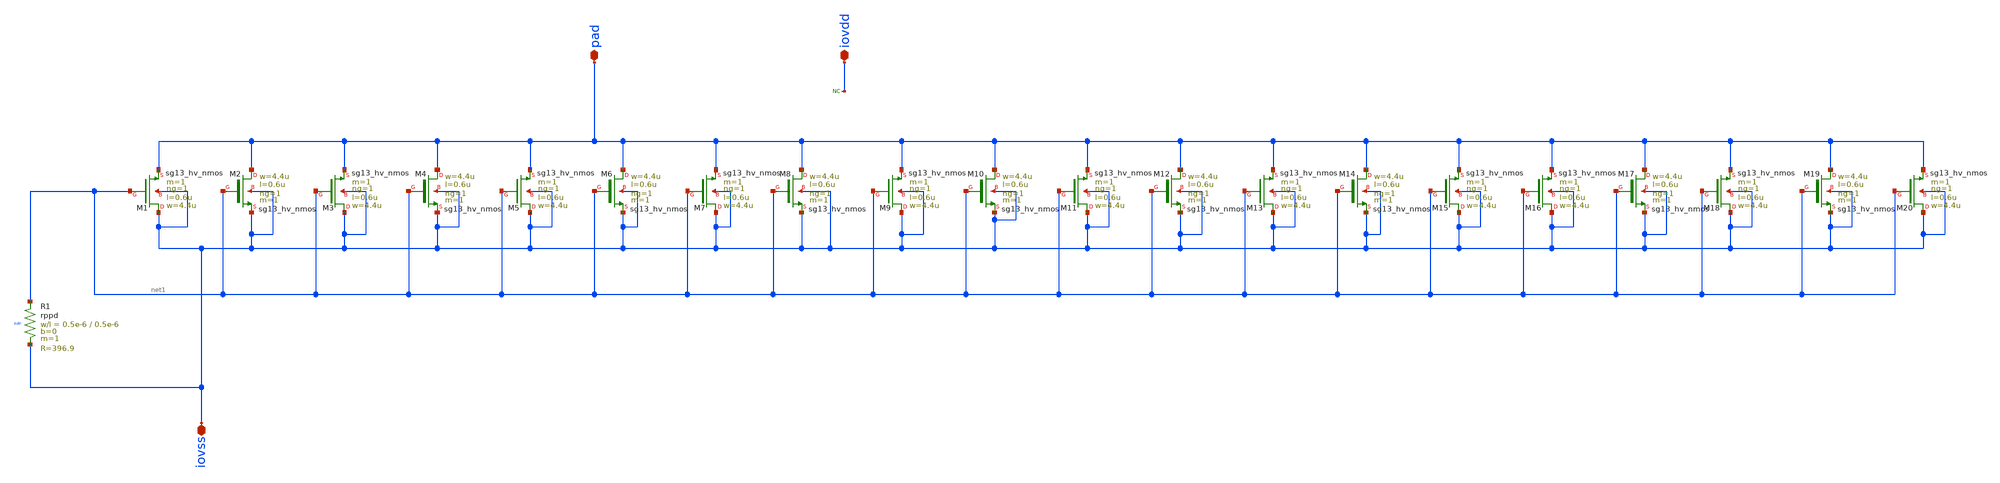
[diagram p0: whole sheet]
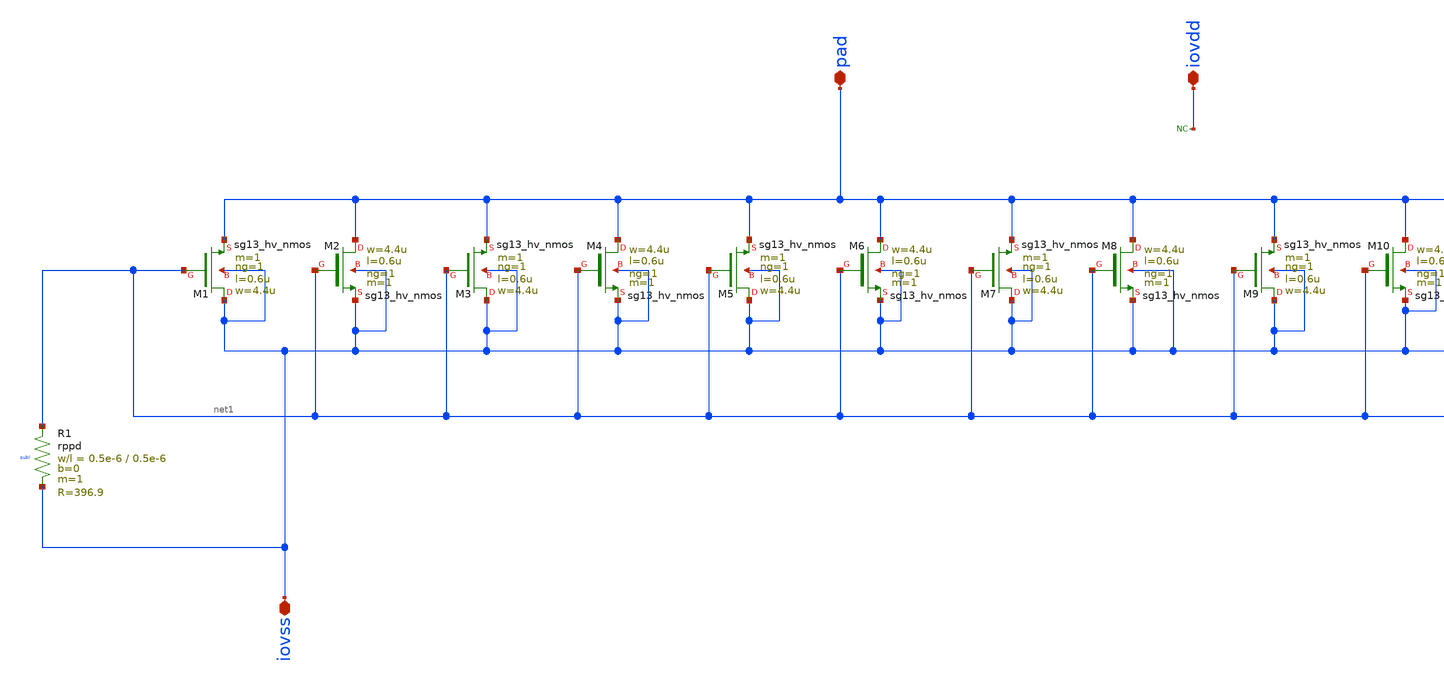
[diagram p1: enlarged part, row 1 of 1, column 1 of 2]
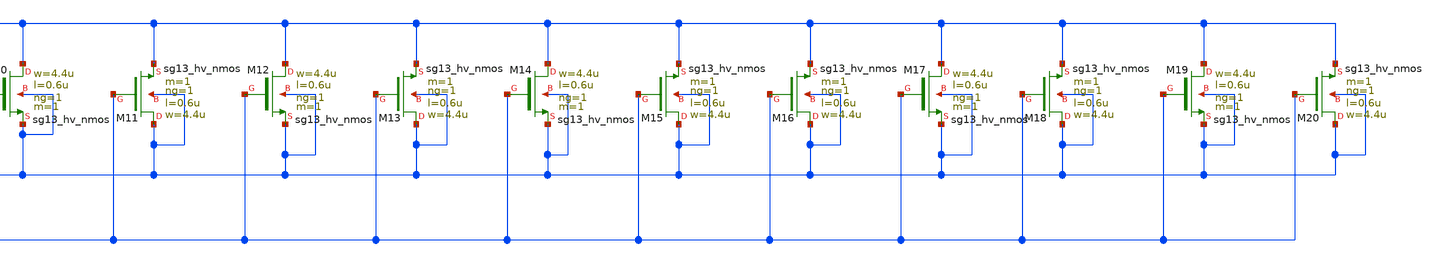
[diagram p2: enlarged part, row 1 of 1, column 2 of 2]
** sch_path: OTA_Telescopic_v3/Schematics_and_Symbols/IOCells/sg13g2_Clamp_N20N0D.sch
**.subckt sg13g2_Clamp_N20N0D iovss pad iovdd
*.iopin iovss
*.iopin pad
*.iopin iovdd
XM1 iovss net1 pad iovss sg13_hv_nmos w=4.4u l=0.6u ng=1 m=1 mm_ok=1
XM2 pad net1 iovss iovss sg13_hv_nmos w=4.4u l=0.6u ng=1 m=1 mm_ok=1
XM3 iovss net1 pad iovss sg13_hv_nmos w=4.4u l=0.6u ng=1 m=1 mm_ok=1
XM4 pad net1 iovss iovss sg13_hv_nmos w=4.4u l=0.6u ng=1 m=1 mm_ok=1
XM5 iovss net1 pad iovss sg13_hv_nmos w=4.4u l=0.6u ng=1 m=1 mm_ok=1
XM6 pad net1 iovss iovss sg13_hv_nmos w=4.4u l=0.6u ng=1 m=1 mm_ok=1
XM7 iovss net1 pad iovss sg13_hv_nmos w=4.4u l=0.6u ng=1 m=1 mm_ok=1
XM8 pad net1 iovss iovss sg13_hv_nmos w=4.4u l=0.6u ng=1 m=1 mm_ok=1
XM9 iovss net1 pad iovss sg13_hv_nmos w=4.4u l=0.6u ng=1 m=1 mm_ok=1
XM10 pad net1 iovss iovss sg13_hv_nmos w=4.4u l=0.6u ng=1 m=1 mm_ok=1
XM11 iovss net1 pad iovss sg13_hv_nmos w=4.4u l=0.6u ng=1 m=1 mm_ok=1
XM12 pad net1 iovss iovss sg13_hv_nmos w=4.4u l=0.6u ng=1 m=1 mm_ok=1
XM13 iovss net1 pad iovss sg13_hv_nmos w=4.4u l=0.6u ng=1 m=1 mm_ok=1
XM14 pad net1 iovss iovss sg13_hv_nmos w=4.4u l=0.6u ng=1 m=1 mm_ok=1
XM15 iovss net1 pad iovss sg13_hv_nmos w=4.4u l=0.6u ng=1 m=1 mm_ok=1
XM16 iovss net1 pad iovss sg13_hv_nmos w=4.4u l=0.6u ng=1 m=1 mm_ok=1
XM17 pad net1 iovss iovss sg13_hv_nmos w=4.4u l=0.6u ng=1 m=1 mm_ok=1
XM18 iovss net1 pad iovss sg13_hv_nmos w=4.4u l=0.6u ng=1 m=1 mm_ok=1
XM19 pad net1 iovss iovss sg13_hv_nmos w=4.4u l=0.6u ng=1 m=1 mm_ok=1
XM20 iovss net1 pad iovss sg13_hv_nmos w=4.4u l=0.6u ng=1 m=1 mm_ok=1
XR1 net1 iovss sub! rppd w=0.5e-6 l=0.5e-6 m=1 b=0 mm_ok=1
* noconn iovdd
**.ends
.end
